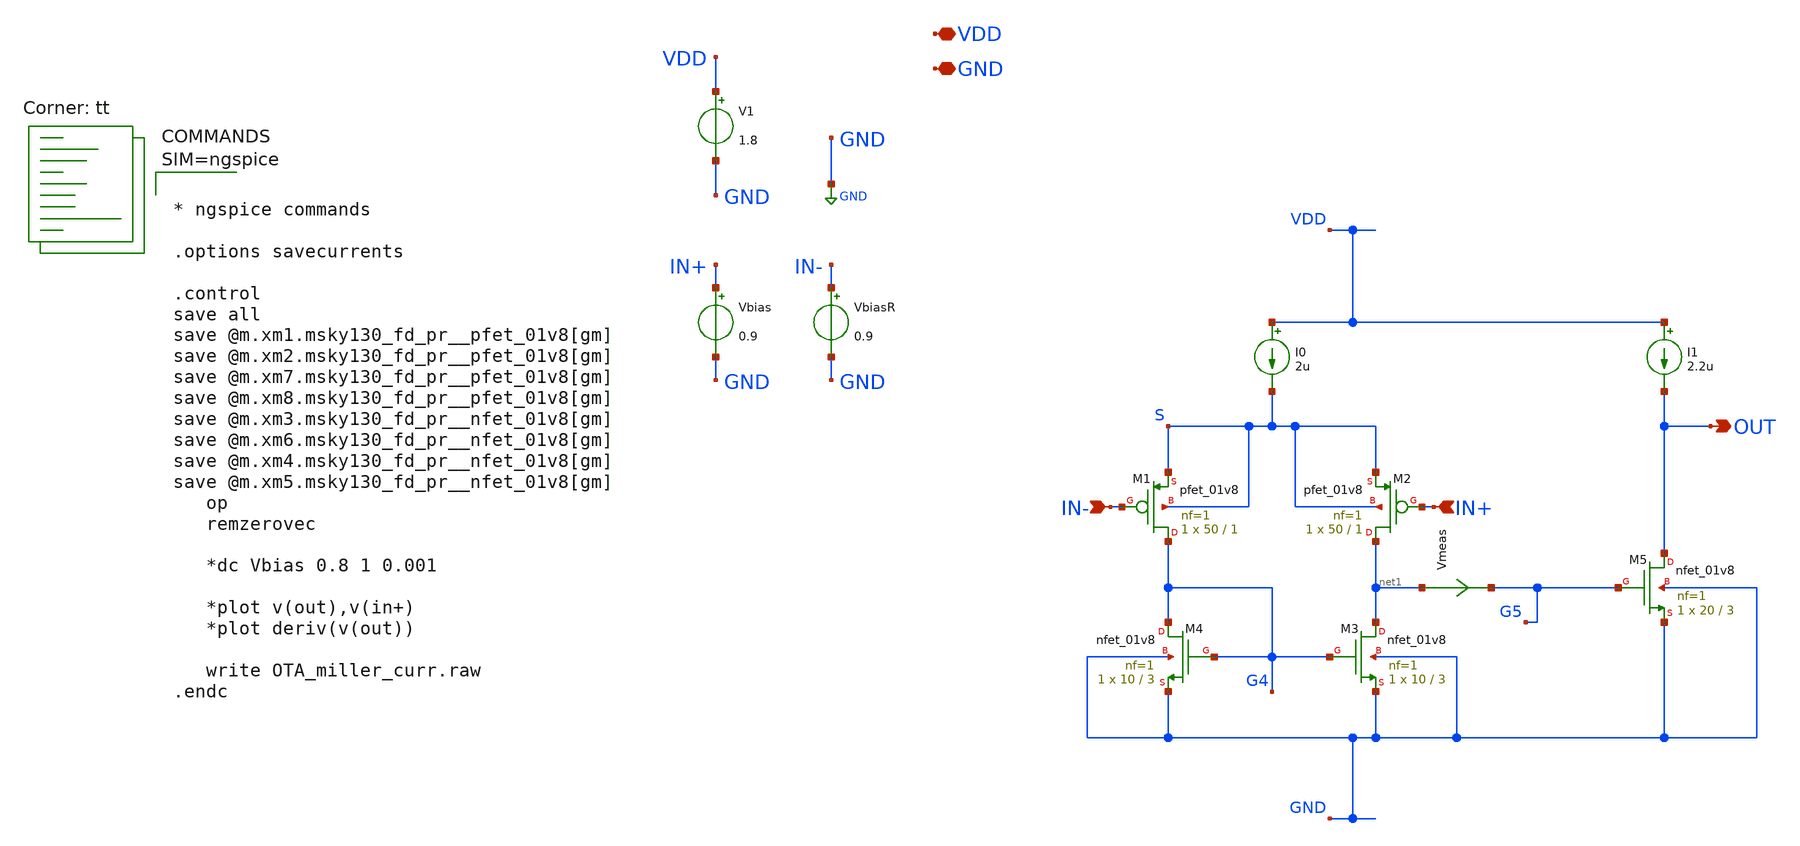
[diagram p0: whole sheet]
** sch_path: xschem/OTA_miller_curr.sch
**.subckt OTA_miller_curr VDD GND IN+ IN- OUT
*.iopin VDD
*.iopin GND
*.ipin IN+
*.ipin IN-
*.opin OUT
XM1 G4 IN- S S sky130_fd_pr__pfet_01v8 L=1 W=50 nf=1 ad='int((nf+1)/2) * W/nf * 0.29' as='int((nf+2)/2) * W/nf * 0.29'
+ pd='2*int((nf+1)/2) * (W/nf + 0.29)' ps='2*int((nf+2)/2) * (W/nf + 0.29)' nrd='0.29 / W' nrs='0.29 / W'
+ sa=0 sb=0 sd=0 mult=1 m=1
XM2 net1 IN+ S S sky130_fd_pr__pfet_01v8 L=1 W=50 nf=1 ad='int((nf+1)/2) * W/nf * 0.29' as='int((nf+2)/2) * W/nf * 0.29'
+ pd='2*int((nf+1)/2) * (W/nf + 0.29)' ps='2*int((nf+2)/2) * (W/nf + 0.29)' nrd='0.29 / W' nrs='0.29 / W'
+ sa=0 sb=0 sd=0 mult=1 m=1
XM3 net1 G4 GND GND sky130_fd_pr__nfet_01v8 L=3 W=10 nf=1 ad='int((nf+1)/2) * W/nf * 0.29' as='int((nf+2)/2) * W/nf * 0.29'
+ pd='2*int((nf+1)/2) * (W/nf + 0.29)' ps='2*int((nf+2)/2) * (W/nf + 0.29)' nrd='0.29 / W' nrs='0.29 / W'
+ sa=0 sb=0 sd=0 mult=1 m=1
XM4 G4 G4 GND GND sky130_fd_pr__nfet_01v8 L=3 W=10 nf=1 ad='int((nf+1)/2) * W/nf * 0.29' as='int((nf+2)/2) * W/nf * 0.29'
+ pd='2*int((nf+1)/2) * (W/nf + 0.29)' ps='2*int((nf+2)/2) * (W/nf + 0.29)' nrd='0.29 / W' nrs='0.29 / W'
+ sa=0 sb=0 sd=0 mult=1 m=1
XM5 OUT G5 GND GND sky130_fd_pr__nfet_01v8 L=3 W=20 nf=1 ad='int((nf+1)/2) * W/nf * 0.29' as='int((nf+2)/2) * W/nf * 0.29'
+ pd='2*int((nf+1)/2) * (W/nf + 0.29)' ps='2*int((nf+2)/2) * (W/nf + 0.29)' nrd='0.29 / W' nrs='0.29 / W'
+ sa=0 sb=0 sd=0 mult=1 m=1
I0 VDD S 2u
V1 VDD GND 1.8
Vbias IN+ GND 0.9
VbiasR IN- GND 0.9
I1 VDD OUT 2.2u
Vmeas net1 G5 0
.save i(vmeas)
**** begin user architecture code



* ngspice commands

.options savecurrents

.control
save all
save @m.xm1.msky130_fd_pr__pfet_01v8[gm]
save @m.xm2.msky130_fd_pr__pfet_01v8[gm]
save @m.xm7.msky130_fd_pr__pfet_01v8[gm]
save @m.xm8.msky130_fd_pr__pfet_01v8[gm]
save @m.xm3.msky130_fd_pr__nfet_01v8[gm]
save @m.xm6.msky130_fd_pr__nfet_01v8[gm]
save @m.xm4.msky130_fd_pr__nfet_01v8[gm]
save @m.xm5.msky130_fd_pr__nfet_01v8[gm]
   op
   remzerovec

   *dc Vbias 0.8 1 0.001

   *plot v(out),v(in+)
   *plot deriv(v(out))

   write OTA_miller_curr.raw
.endc




.lib $::SKYWATER_MODELS/sky130.lib.spice tt
**** end user architecture code
**.ends
.GLOBAL GND
.end
